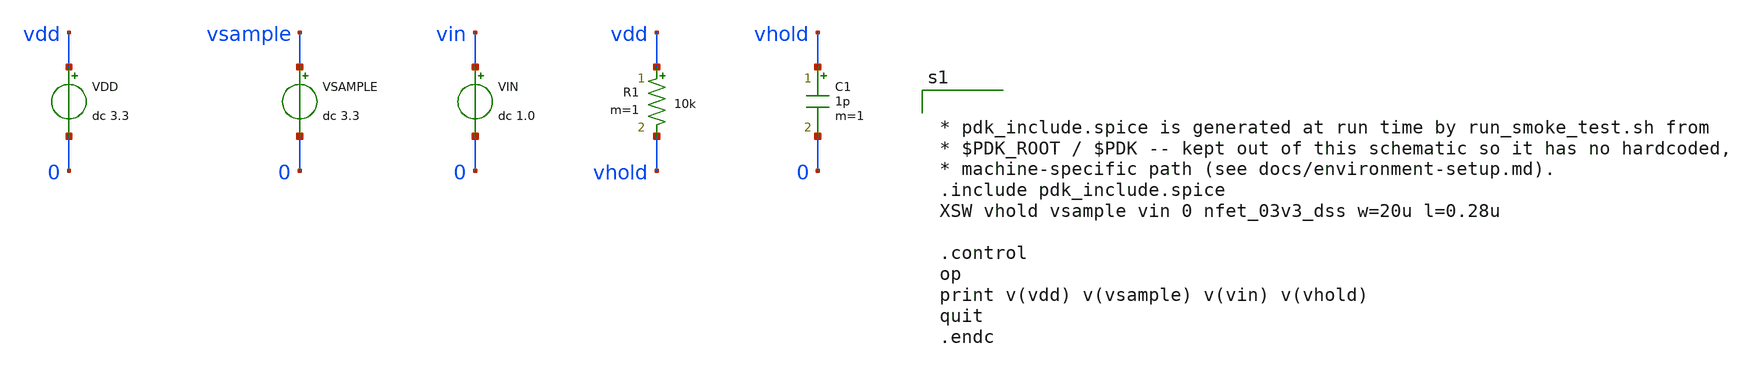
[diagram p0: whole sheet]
** sch_path: design/smoke_test.sch
**.subckt smoke_test
VDD vdd 0 dc 3.3
VSAMPLE vsample 0 dc 3.3
VIN vin 0 dc 1.0
R1 vdd vhold 10k m=1
C1 vhold 0 1p m=1
**** begin user architecture code


* pdk_include.spice is generated at run time by run_smoke_test.sh from
* $PDK_ROOT / $PDK -- kept out of this schematic so it has no hardcoded,
* machine-specific path (see docs/environment-setup.md).
.include pdk_include.spice
XSW vhold vsample vin 0 nfet_03v3_dss w=20u l=0.28u

.control
op
print v(vdd) v(vsample) v(vin) v(vhold)
quit
.endc


**** end user architecture code
**.ends
.end
